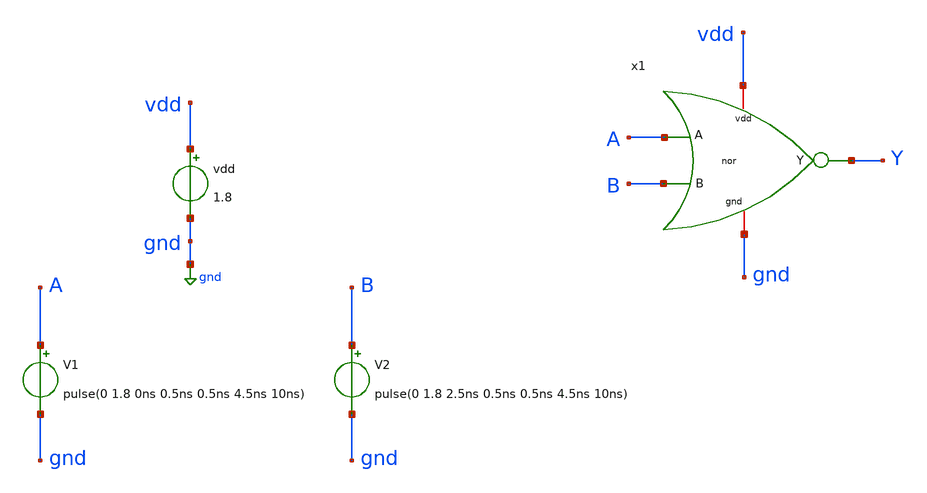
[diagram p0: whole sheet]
** sch_path: LogicGates/nor_tb.sch
**.subckt nor_tb
x1 vdd gnd A B Y nor
vdd vdd gnd 1.8
V1 A gnd pulse(0 1.8 0ns 0.5ns 0.5ns 4.5ns 10ns)
V2 B gnd pulse(0 1.8 2.5ns 0.5ns 0.5ns 4.5ns 10ns)
**** begin user architecture code


.lib /usr/local/share/pdk/sky130A/libs.tech/ngspice/sky130.lib.spice tt
.control
    tran 0.1n 50n
    plot A B
    plot Y
.endc

.save all

**** end user architecture code
**.ends

* expanding   symbol:  LogicGates/nor.sym # of pins=5
** sym_path: LogicGates/nor.sym
** sch_path: LogicGates/nor.sch
.subckt nor vdd gnd A B Y
*.ipin A
*.ipin B
*.iopin vdd
*.iopin gnd
*.opin Y
XM1 Y A gnd gnd sky130_fd_pr__nfet_01v8 L=0.15 W=1 nf=1 ad='int((nf+1)/2) * W/nf * 0.29' as='int((nf+2)/2) * W/nf * 0.29'
+ pd='2*int((nf+1)/2) * (W/nf + 0.29)' ps='2*int((nf+2)/2) * (W/nf + 0.29)' nrd='0.29 / W' nrs='0.29 / W'
+ sa=0 sb=0 sd=0 mult=1 m=1
XM2 Y B gnd gnd sky130_fd_pr__nfet_01v8 L=0.15 W=1 nf=1 ad='int((nf+1)/2) * W/nf * 0.29' as='int((nf+2)/2) * W/nf * 0.29'
+ pd='2*int((nf+1)/2) * (W/nf + 0.29)' ps='2*int((nf+2)/2) * (W/nf + 0.29)' nrd='0.29 / W' nrs='0.29 / W'
+ sa=0 sb=0 sd=0 mult=1 m=1
XM3 net1 A vdd vdd sky130_fd_pr__pfet_01v8 L=0.15 W=2 nf=1 ad='int((nf+1)/2) * W/nf * 0.29' as='int((nf+2)/2) * W/nf * 0.29'
+ pd='2*int((nf+1)/2) * (W/nf + 0.29)' ps='2*int((nf+2)/2) * (W/nf + 0.29)' nrd='0.29 / W' nrs='0.29 / W'
+ sa=0 sb=0 sd=0 mult=1 m=1
XM4 Y B net1 vdd sky130_fd_pr__pfet_01v8 L=0.15 W=2 nf=1 ad='int((nf+1)/2) * W/nf * 0.29' as='int((nf+2)/2) * W/nf * 0.29'
+ pd='2*int((nf+1)/2) * (W/nf + 0.29)' ps='2*int((nf+2)/2) * (W/nf + 0.29)' nrd='0.29 / W' nrs='0.29 / W'
+ sa=0 sb=0 sd=0 mult=1 m=1
.ends

.GLOBAL gnd
.end
